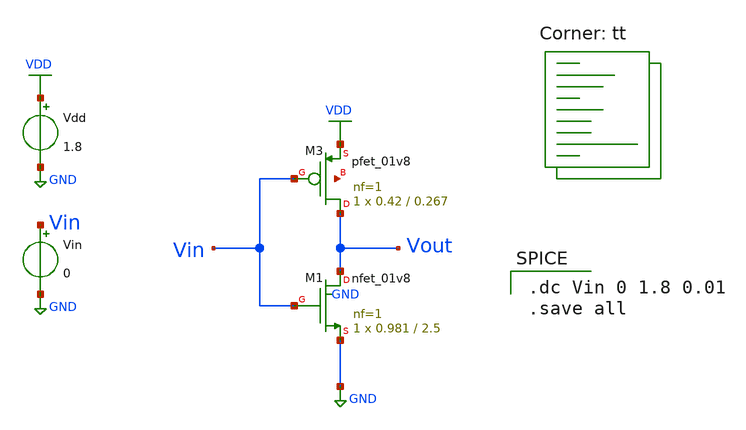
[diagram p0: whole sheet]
** sch_path: vdd1.8V/inverter_sat_7.sch
**.subckt inverter_sat_7
Vdd VDD GND 1.8
XM1 Vout Vin GND GND sky130_fd_pr__nfet_01v8 L=2.5 W=0.981 nf=1 ad='int((nf+1)/2) * W/nf * 0.29' as='int((nf+2)/2) * W/nf * 0.29'
+ pd='2*int((nf+1)/2) * (W/nf + 0.29)' ps='2*int((nf+2)/2) * (W/nf + 0.29)' nrd='0.29 / W' nrs='0.29 / W'
+ sa=0 sb=0 sd=0 mult=1 m=1
Vin Vin GND 0
XM3 Vout Vin VDD net1 sky130_fd_pr__pfet_01v8 L=0.267 W=0.42 nf=1 ad='int((nf+1)/2) * W/nf * 0.29' as='int((nf+2)/2) * W/nf * 0.29'
+ pd='2*int((nf+1)/2) * (W/nf + 0.29)' ps='2*int((nf+2)/2) * (W/nf + 0.29)' nrd='0.29 / W' nrs='0.29 / W'
+ sa=0 sb=0 sd=0 mult=1 m=1
**** begin user architecture code

.dc Vin 0 1.8 0.01
.save all

.lib $::SKYWATER_MODELS/sky130.lib.spice tt
**** end user architecture code
**.ends
.GLOBAL GND
.GLOBAL VDD
.end
